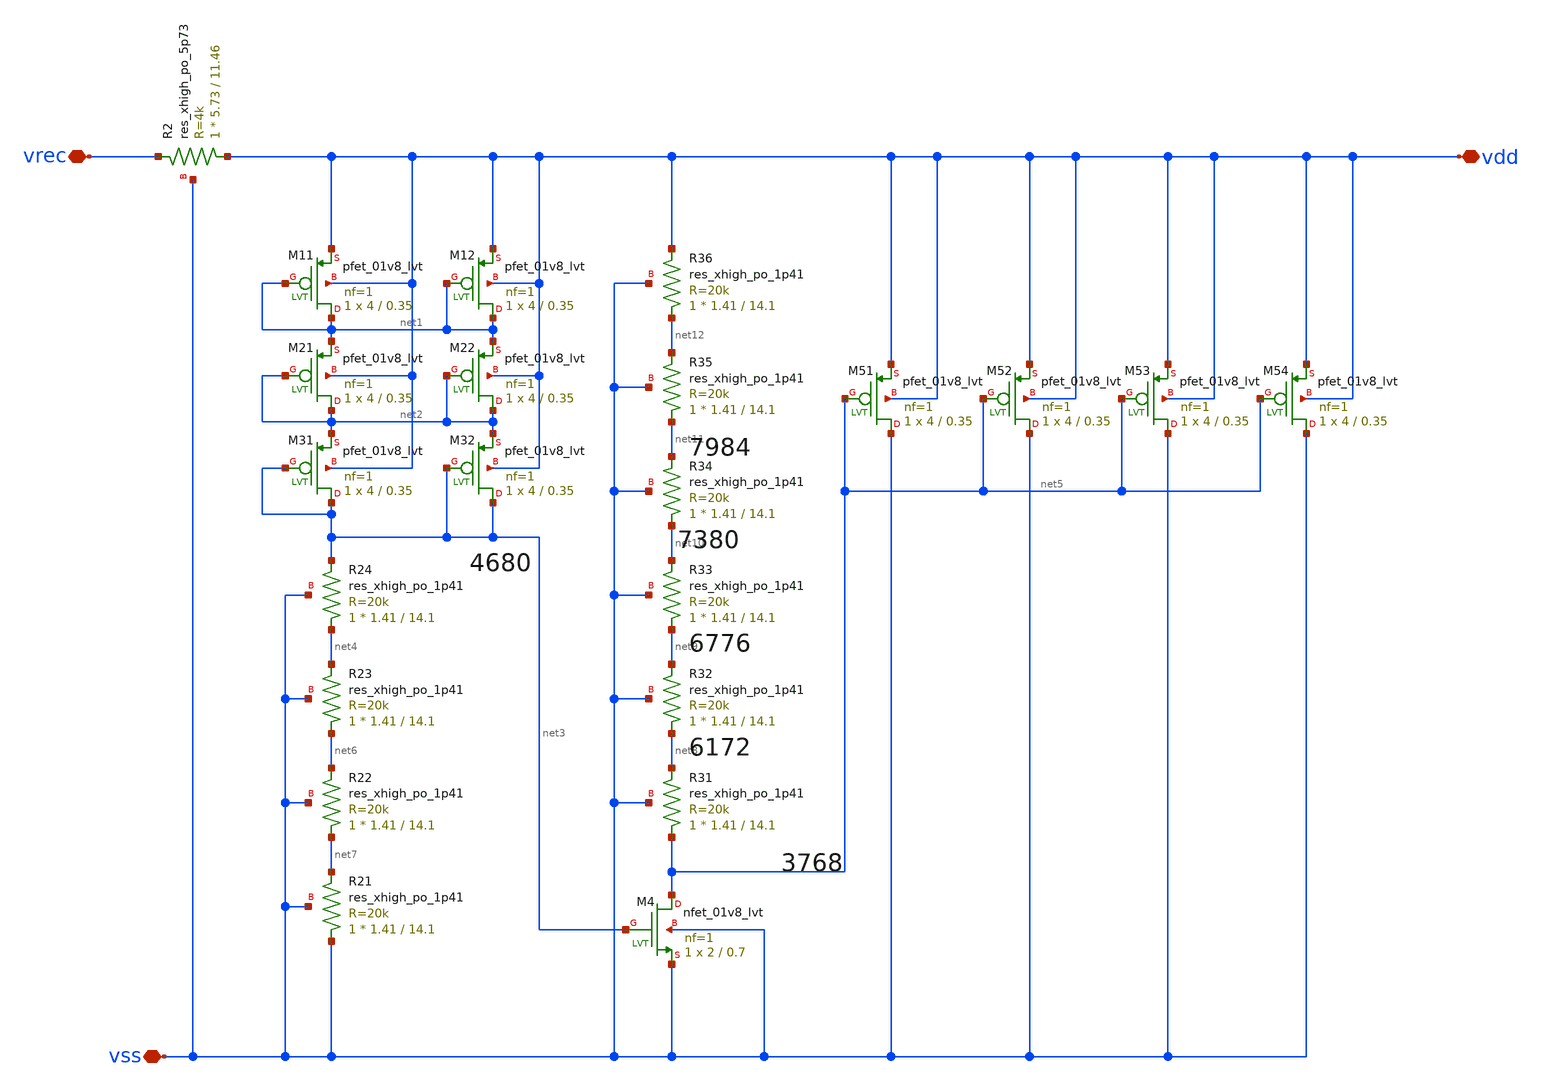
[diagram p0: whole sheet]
** sch_path: XSCHEM/For_Layout/voltage_limiter.sch
**.subckt voltage_limiter vss vrec vdd
*.iopin vss
*.iopin vrec
*.iopin vdd
XM4 net5 net3 vss vss sky130_fd_pr__nfet_01v8_lvt L=0.7 W=2 nf=1 ad='int((nf+1)/2) * W/nf * 0.29' as='int((nf+2)/2) * W/nf * 0.29'
+ pd='2*int((nf+1)/2) * (W/nf + 0.29)' ps='2*int((nf+2)/2) * (W/nf + 0.29)' nrd='0.29 / W' nrs='0.29 / W'
+ sa=0 sb=0 sd=0 mult=1 m=1
XM51 vss net5 vdd vdd sky130_fd_pr__pfet_01v8_lvt L=0.35 W=4 nf=1 ad='int((nf+1)/2) * W/nf * 0.29' as='int((nf+2)/2) * W/nf * 0.29'
+ pd='2*int((nf+1)/2) * (W/nf + 0.29)' ps='2*int((nf+2)/2) * (W/nf + 0.29)' nrd='0.29 / W' nrs='0.29 / W'
+ sa=0 sb=0 sd=0 mult=1 m=1
XM11 net1 net1 vdd vdd sky130_fd_pr__pfet_01v8_lvt L=0.35 W=4 nf=1 ad='int((nf+1)/2) * W/nf * 0.29' as='int((nf+2)/2) * W/nf * 0.29'
+ pd='2*int((nf+1)/2) * (W/nf + 0.29)' ps='2*int((nf+2)/2) * (W/nf + 0.29)' nrd='0.29 / W' nrs='0.29 / W'
+ sa=0 sb=0 sd=0 mult=1 m=1
XM21 net2 net2 net1 vdd sky130_fd_pr__pfet_01v8_lvt L=0.35 W=4 nf=1 ad='int((nf+1)/2) * W/nf * 0.29'
+ as='int((nf+2)/2) * W/nf * 0.29' pd='2*int((nf+1)/2) * (W/nf + 0.29)' ps='2*int((nf+2)/2) * (W/nf + 0.29)'
+ nrd='0.29 / W' nrs='0.29 / W' sa=0 sb=0 sd=0 mult=1 m=1
XM31 net3 net3 net2 vdd sky130_fd_pr__pfet_01v8_lvt L=0.35 W=4 nf=1 ad='int((nf+1)/2) * W/nf * 0.29'
+ as='int((nf+2)/2) * W/nf * 0.29' pd='2*int((nf+1)/2) * (W/nf + 0.29)' ps='2*int((nf+2)/2) * (W/nf + 0.29)'
+ nrd='0.29 / W' nrs='0.29 / W' sa=0 sb=0 sd=0 mult=1 m=1
XM12 net1 net1 vdd vdd sky130_fd_pr__pfet_01v8_lvt L=0.35 W=4 nf=1 ad='int((nf+1)/2) * W/nf * 0.29' as='int((nf+2)/2) * W/nf * 0.29'
+ pd='2*int((nf+1)/2) * (W/nf + 0.29)' ps='2*int((nf+2)/2) * (W/nf + 0.29)' nrd='0.29 / W' nrs='0.29 / W'
+ sa=0 sb=0 sd=0 mult=1 m=1
XM22 net2 net2 net1 vdd sky130_fd_pr__pfet_01v8_lvt L=0.35 W=4 nf=1 ad='int((nf+1)/2) * W/nf * 0.29'
+ as='int((nf+2)/2) * W/nf * 0.29' pd='2*int((nf+1)/2) * (W/nf + 0.29)' ps='2*int((nf+2)/2) * (W/nf + 0.29)'
+ nrd='0.29 / W' nrs='0.29 / W' sa=0 sb=0 sd=0 mult=1 m=1
XM32 net3 net3 net2 vdd sky130_fd_pr__pfet_01v8_lvt L=0.35 W=4 nf=1 ad='int((nf+1)/2) * W/nf * 0.29'
+ as='int((nf+2)/2) * W/nf * 0.29' pd='2*int((nf+1)/2) * (W/nf + 0.29)' ps='2*int((nf+2)/2) * (W/nf + 0.29)'
+ nrd='0.29 / W' nrs='0.29 / W' sa=0 sb=0 sd=0 mult=1 m=1
XM52 vss net5 vdd vdd sky130_fd_pr__pfet_01v8_lvt L=0.35 W=4 nf=1 ad='int((nf+1)/2) * W/nf * 0.29' as='int((nf+2)/2) * W/nf * 0.29'
+ pd='2*int((nf+1)/2) * (W/nf + 0.29)' ps='2*int((nf+2)/2) * (W/nf + 0.29)' nrd='0.29 / W' nrs='0.29 / W'
+ sa=0 sb=0 sd=0 mult=1 m=1
XM53 vss net5 vdd vdd sky130_fd_pr__pfet_01v8_lvt L=0.35 W=4 nf=1 ad='int((nf+1)/2) * W/nf * 0.29' as='int((nf+2)/2) * W/nf * 0.29'
+ pd='2*int((nf+1)/2) * (W/nf + 0.29)' ps='2*int((nf+2)/2) * (W/nf + 0.29)' nrd='0.29 / W' nrs='0.29 / W'
+ sa=0 sb=0 sd=0 mult=1 m=1
XM54 vss net5 vdd vdd sky130_fd_pr__pfet_01v8_lvt L=0.35 W=4 nf=1 ad='int((nf+1)/2) * W/nf * 0.29' as='int((nf+2)/2) * W/nf * 0.29'
+ pd='2*int((nf+1)/2) * (W/nf + 0.29)' ps='2*int((nf+2)/2) * (W/nf + 0.29)' nrd='0.29 / W' nrs='0.29 / W'
+ sa=0 sb=0 sd=0 mult=1 m=1
XR24 net4 net3 vss sky130_fd_pr__res_xhigh_po_1p41 L=14.1 mult=1 m=1
XR23 net6 net4 vss sky130_fd_pr__res_xhigh_po_1p41 L=14.1 mult=1 m=1
XR22 net7 net6 vss sky130_fd_pr__res_xhigh_po_1p41 L=14.1 mult=1 m=1
XR21 vss net7 vss sky130_fd_pr__res_xhigh_po_1p41 L=14.1 mult=1 m=1
XR36 net12 vdd vss sky130_fd_pr__res_xhigh_po_1p41 L=14.1 mult=1 m=1
XR35 net11 net12 vss sky130_fd_pr__res_xhigh_po_1p41 L=14.1 mult=1 m=1
XR34 net10 net11 vss sky130_fd_pr__res_xhigh_po_1p41 L=14.1 mult=1 m=1
XR33 net9 net10 vss sky130_fd_pr__res_xhigh_po_1p41 L=14.1 mult=1 m=1
XR32 net8 net9 vss sky130_fd_pr__res_xhigh_po_1p41 L=14.1 mult=1 m=1
XR31 net5 net8 vss sky130_fd_pr__res_xhigh_po_1p41 L=14.1 mult=1 m=1
XR2 vdd vrec vss sky130_fd_pr__res_xhigh_po_5p73 L=11.46 mult=1 m=1
**.ends
.end
